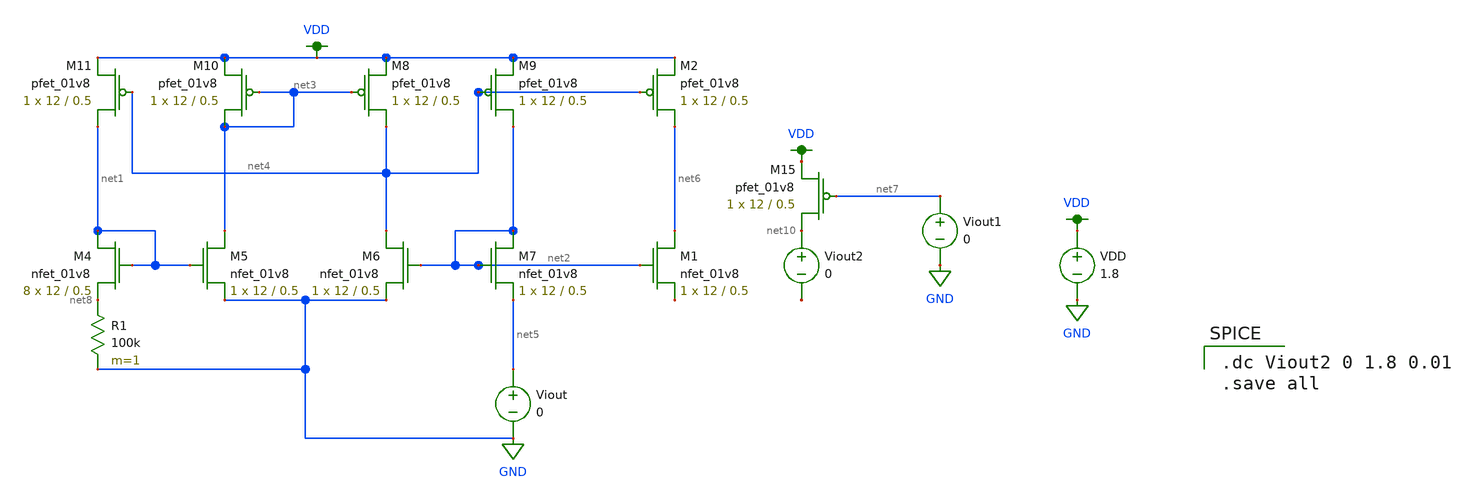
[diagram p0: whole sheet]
** sch_path: schematics/bias/test_current_bias_raw_range.sch
**.subckt test_current_bias_raw_range
XM4 net1 net1 net8 GND sky130_fd_pr__nfet_01v8 L=0.5 W=12 nf=1 ad='int((nf+1)/2) * W/nf * 0.29' as='int((nf+2)/2) * W/nf * 0.29'
+ pd='2*int((nf+1)/2) * (W/nf + 0.29)' ps='2*int((nf+2)/2) * (W/nf + 0.29)' nrd='0.29 / W' nrs='0.29 / W'
+ sa=0 sb=0 sd=0 mult=8 m=8
XM5 net3 net1 GND GND sky130_fd_pr__nfet_01v8 L=0.5 W=12 nf=1 ad='int((nf+1)/2) * W/nf * 0.29' as='int((nf+2)/2) * W/nf * 0.29'
+ pd='2*int((nf+1)/2) * (W/nf + 0.29)' ps='2*int((nf+2)/2) * (W/nf + 0.29)' nrd='0.29 / W' nrs='0.29 / W'
+ sa=0 sb=0 sd=0 mult=1 m=1
XM6 net4 net2 GND GND sky130_fd_pr__nfet_01v8 L=0.5 W=12 nf=1 ad='int((nf+1)/2) * W/nf * 0.29' as='int((nf+2)/2) * W/nf * 0.29'
+ pd='2*int((nf+1)/2) * (W/nf + 0.29)' ps='2*int((nf+2)/2) * (W/nf + 0.29)' nrd='0.29 / W' nrs='0.29 / W'
+ sa=0 sb=0 sd=0 mult=1 m=1
XM7 net2 net2 net5 GND sky130_fd_pr__nfet_01v8 L=0.5 W=12 nf=1 ad='int((nf+1)/2) * W/nf * 0.29' as='int((nf+2)/2) * W/nf * 0.29'
+ pd='2*int((nf+1)/2) * (W/nf + 0.29)' ps='2*int((nf+2)/2) * (W/nf + 0.29)' nrd='0.29 / W' nrs='0.29 / W'
+ sa=0 sb=0 sd=0 mult=1 m=1
R1 net8 GND 100k m=1
XM8 net4 net3 VDD VDD sky130_fd_pr__pfet_01v8 L=0.5 W=12 nf=1 ad='int((nf+1)/2) * W/nf * 0.29' as='int((nf+2)/2) * W/nf * 0.29'
+ pd='2*int((nf+1)/2) * (W/nf + 0.29)' ps='2*int((nf+2)/2) * (W/nf + 0.29)' nrd='0.29 / W' nrs='0.29 / W'
+ sa=0 sb=0 sd=0 mult=1 m=1
XM9 net2 net4 VDD VDD sky130_fd_pr__pfet_01v8 L=0.5 W=12 nf=1 ad='int((nf+1)/2) * W/nf * 0.29' as='int((nf+2)/2) * W/nf * 0.29'
+ pd='2*int((nf+1)/2) * (W/nf + 0.29)' ps='2*int((nf+2)/2) * (W/nf + 0.29)' nrd='0.29 / W' nrs='0.29 / W'
+ sa=0 sb=0 sd=0 mult=1 m=1
XM10 net3 net3 VDD VDD sky130_fd_pr__pfet_01v8 L=0.5 W=12 nf=1 ad='int((nf+1)/2) * W/nf * 0.29' as='int((nf+2)/2) * W/nf * 0.29'
+ pd='2*int((nf+1)/2) * (W/nf + 0.29)' ps='2*int((nf+2)/2) * (W/nf + 0.29)' nrd='0.29 / W' nrs='0.29 / W'
+ sa=0 sb=0 sd=0 mult=1 m=1
XM11 net1 net4 VDD VDD sky130_fd_pr__pfet_01v8 L=0.5 W=12 nf=1 ad='int((nf+1)/2) * W/nf * 0.29' as='int((nf+2)/2) * W/nf * 0.29'
+ pd='2*int((nf+1)/2) * (W/nf + 0.29)' ps='2*int((nf+2)/2) * (W/nf + 0.29)' nrd='0.29 / W' nrs='0.29 / W'
+ sa=0 sb=0 sd=0 mult=1 m=1
Viout net5 GND 0
VDD VDD GND 1.8
XM1 net6 net2 net9 GND sky130_fd_pr__nfet_01v8 L=0.5 W=12 nf=1 ad='int((nf+1)/2) * W/nf * 0.29' as='int((nf+2)/2) * W/nf * 0.29'
+ pd='2*int((nf+1)/2) * (W/nf + 0.29)' ps='2*int((nf+2)/2) * (W/nf + 0.29)' nrd='0.29 / W' nrs='0.29 / W'
+ sa=0 sb=0 sd=0 mult=1 m=1
XM2 net6 net4 VDD VDD sky130_fd_pr__pfet_01v8 L=0.5 W=12 nf=1 ad='int((nf+1)/2) * W/nf * 0.29' as='int((nf+2)/2) * W/nf * 0.29'
+ pd='2*int((nf+1)/2) * (W/nf + 0.29)' ps='2*int((nf+2)/2) * (W/nf + 0.29)' nrd='0.29 / W' nrs='0.29 / W'
+ sa=0 sb=0 sd=0 mult=1 m=1
XM15 net10 net7 VDD VDD sky130_fd_pr__pfet_01v8 L=0.5 W=12 nf=1 ad='int((nf+1)/2) * W/nf * 0.29' as='int((nf+2)/2) * W/nf * 0.29'
+ pd='2*int((nf+1)/2) * (W/nf + 0.29)' ps='2*int((nf+2)/2) * (W/nf + 0.29)' nrd='0.29 / W' nrs='0.29 / W'
+ sa=0 sb=0 sd=0 mult=1 m=1
Viout1 net7 GND 0
Viout2 net10 net11 0
**** begin user architecture code

.option wnflag=1
.param MC_SWITCH=0.0
.lib ~/skywater/skywater-pdk/libraries/sky130_fd_pr_ngspice/latest/models/sky130.lib.spice tt


.dc Viout2 0 1.8 0.01
.save all

**** end user architecture code
**.ends
.GLOBAL GND
.GLOBAL VDD
.end
